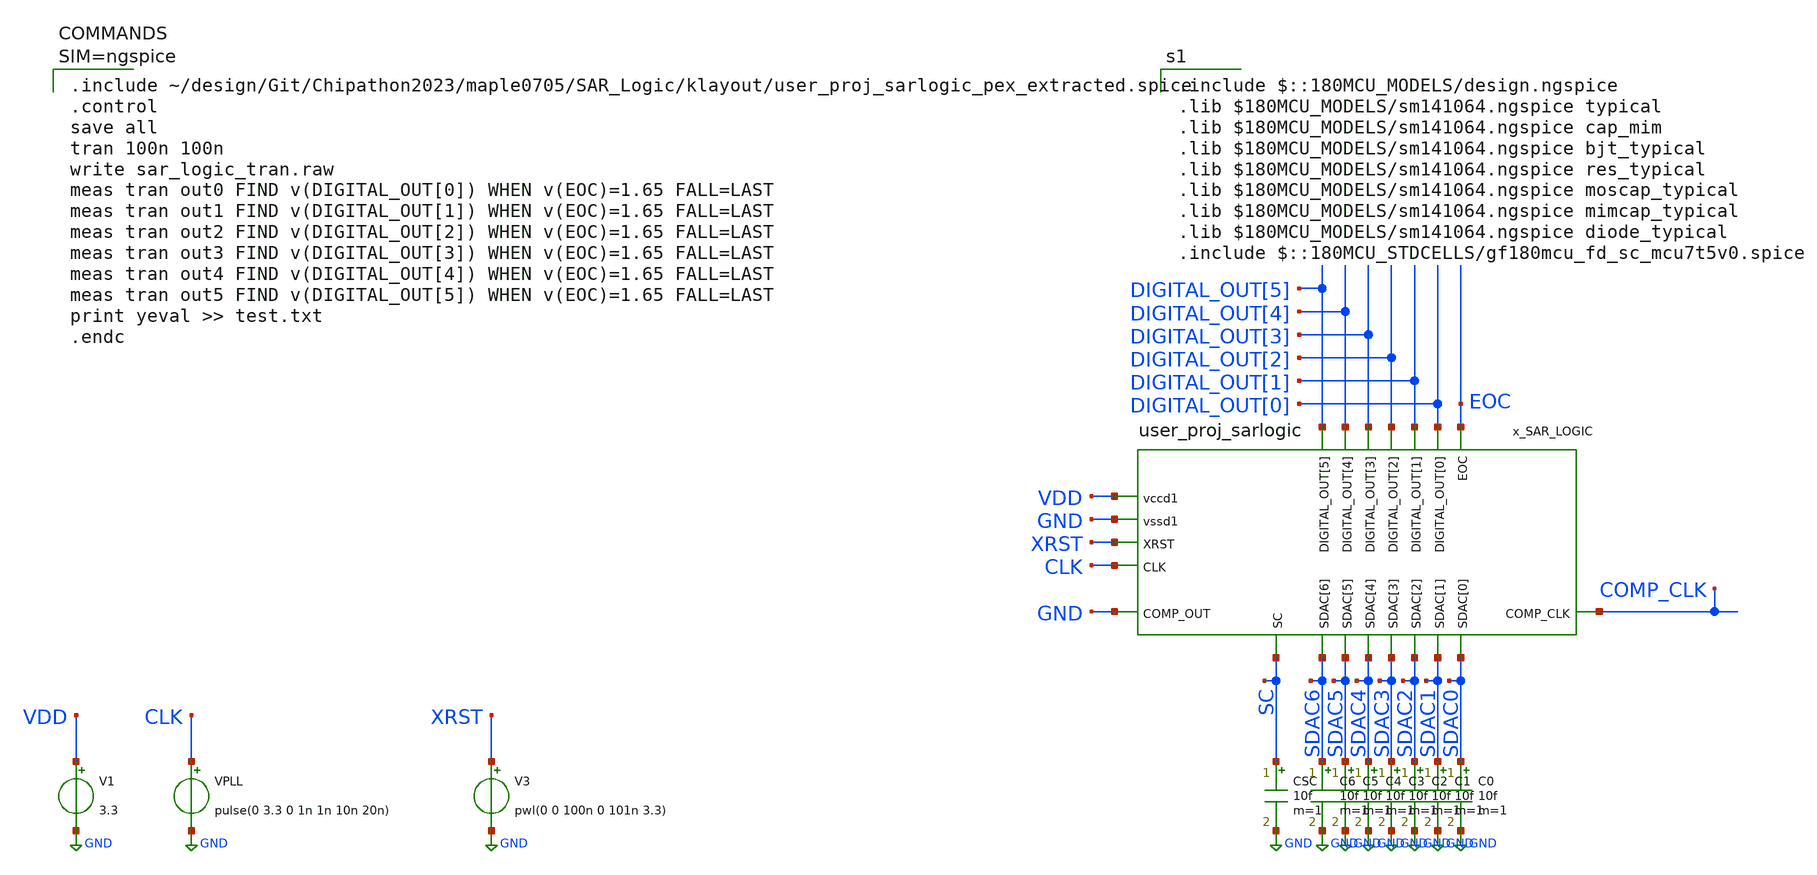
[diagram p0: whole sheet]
** sch_path: maple0705/SAR_Logic/xschem/tran_sar_logic.sch
**.subckt tran_sar_logic
C0 SDAC0 GND 10f m=1
V1 VDD GND 3.3
VPLL CLK GND pulse(0 3.3 0 1n 1n 10n 20n)
x_SAR_LOGIC CLK COMP_CLK GND DIGITAL_OUT[0] DIGITAL_OUT[1] DIGITAL_OUT[2] DIGITAL_OUT[3]
+ DIGITAL_OUT[4] DIGITAL_OUT[5] EOC XRST SC SDAC0 SDAC1 SDAC2 SDAC3 SDAC4 SDAC5 SDAC6 VDD GND user_proj_sarlogic
V3 XRST GND pwl(0 0 100n 0 101n 3.3)
C1 SDAC1 GND 10f m=1
C2 SDAC2 GND 10f m=1
C3 SDAC3 GND 10f m=1
C4 SDAC4 GND 10f m=1
C5 SDAC5 GND 10f m=1
C6 SDAC6 GND 10f m=1
CSC SC GND 10f m=1
**** begin user architecture code


.include ~/design/Git/Chipathon2023/maple0705/SAR_Logic/klayout/user_proj_sarlogic_pex_extracted.spice
.control
save all
tran 100n 100n
write sar_logic_tran.raw
meas tran out0 FIND v(DIGITAL_OUT[0]) WHEN v(EOC)=1.65 FALL=LAST
meas tran out1 FIND v(DIGITAL_OUT[1]) WHEN v(EOC)=1.65 FALL=LAST
meas tran out2 FIND v(DIGITAL_OUT[2]) WHEN v(EOC)=1.65 FALL=LAST
meas tran out3 FIND v(DIGITAL_OUT[3]) WHEN v(EOC)=1.65 FALL=LAST
meas tran out4 FIND v(DIGITAL_OUT[4]) WHEN v(EOC)=1.65 FALL=LAST
meas tran out5 FIND v(DIGITAL_OUT[5]) WHEN v(EOC)=1.65 FALL=LAST
print yeval >> test.txt
.endc



 .include $::180MCU_MODELS/design.ngspice
.lib $180MCU_MODELS/sm141064.ngspice typical
.lib $180MCU_MODELS/sm141064.ngspice cap_mim
.lib $180MCU_MODELS/sm141064.ngspice bjt_typical
.lib $180MCU_MODELS/sm141064.ngspice res_typical
.lib $180MCU_MODELS/sm141064.ngspice moscap_typical
.lib $180MCU_MODELS/sm141064.ngspice mimcap_typical
.lib $180MCU_MODELS/sm141064.ngspice diode_typical
.include $::180MCU_STDCELLS/gf180mcu_fd_sc_mcu7t5v0.spice
**** end user architecture code
**.ends
.GLOBAL GND
.end
